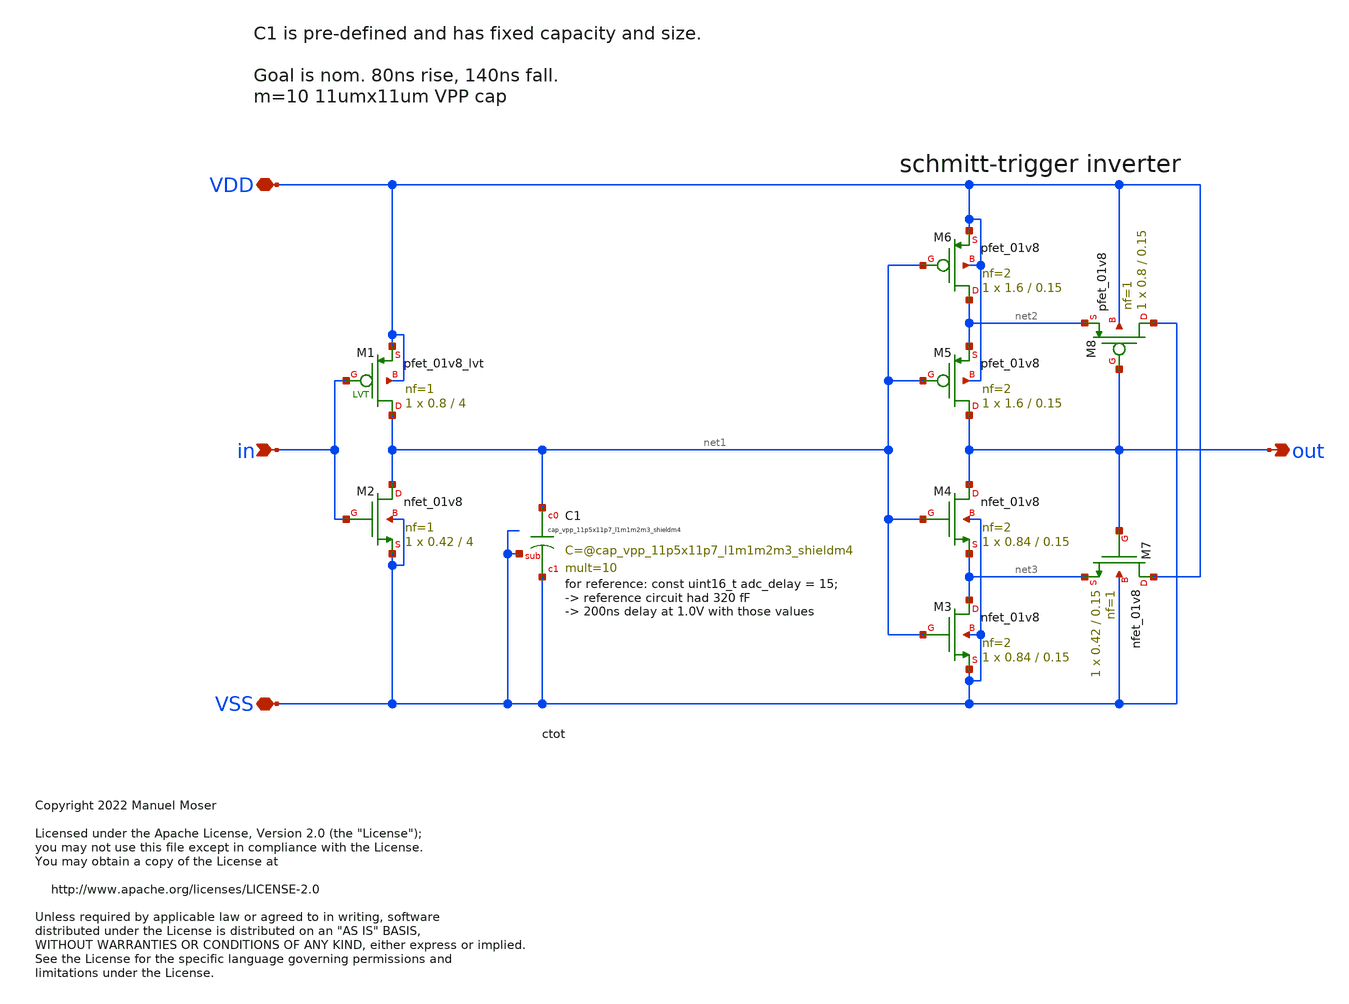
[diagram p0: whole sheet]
** sch_path: xschem/archive/adc_edge_detect_delay/_analog/adc_edge_detect_delay.sch
* Copyright 2022 Manuel Moser
* Licensed under the Apache License, Version 2.0 (the "License");
**.subckt adc_edge_detect_delay VDD VSS in out
*.iopin VDD
*.iopin VSS
*.ipin in
*.opin out
XC1 net1 VSS VSS sky130_fd_pr__cap_vpp_11p5x11p7_l1m1m2m3_shieldm4 mult=10 m=10
XM3 net3 net1 VSS VSS sky130_fd_pr__nfet_01v8 L=0.15 W=0.84 nf=2 ad='int((nf+1)/2) * W/nf * 0.29' as='int((nf+2)/2) * W/nf * 0.29'
+ pd='2*int((nf+1)/2) * (W/nf + 0.29)' ps='2*int((nf+2)/2) * (W/nf + 0.29)' nrd='0.29 / W' nrs='0.29 / W'
+ sa=0 sb=0 sd=0 mult=1 m=1
XM4 out net1 net3 VSS sky130_fd_pr__nfet_01v8 L=0.15 W=0.84 nf=2 ad='int((nf+1)/2) * W/nf * 0.29' as='int((nf+2)/2) * W/nf * 0.29'
+ pd='2*int((nf+1)/2) * (W/nf + 0.29)' ps='2*int((nf+2)/2) * (W/nf + 0.29)' nrd='0.29 / W' nrs='0.29 / W'
+ sa=0 sb=0 sd=0 mult=1 m=1
XM5 out net1 net2 VDD sky130_fd_pr__pfet_01v8 L=0.15 W=1.6 nf=2 ad='int((nf+1)/2) * W/nf * 0.29' as='int((nf+2)/2) * W/nf * 0.29'
+ pd='2*int((nf+1)/2) * (W/nf + 0.29)' ps='2*int((nf+2)/2) * (W/nf + 0.29)' nrd='0.29 / W' nrs='0.29 / W'
+ sa=0 sb=0 sd=0 mult=1 m=1
XM6 net2 net1 VDD VDD sky130_fd_pr__pfet_01v8 L=0.15 W=1.6 nf=2 ad='int((nf+1)/2) * W/nf * 0.29' as='int((nf+2)/2) * W/nf * 0.29'
+ pd='2*int((nf+1)/2) * (W/nf + 0.29)' ps='2*int((nf+2)/2) * (W/nf + 0.29)' nrd='0.29 / W' nrs='0.29 / W'
+ sa=0 sb=0 sd=0 mult=1 m=1
XM7 VDD out net3 VSS sky130_fd_pr__nfet_01v8 L=0.15 W=0.42 nf=1 ad='int((nf+1)/2) * W/nf * 0.29' as='int((nf+2)/2) * W/nf * 0.29'
+ pd='2*int((nf+1)/2) * (W/nf + 0.29)' ps='2*int((nf+2)/2) * (W/nf + 0.29)' nrd='0.29 / W' nrs='0.29 / W'
+ sa=0 sb=0 sd=0 mult=1 m=1
XM8 VSS out net2 VDD sky130_fd_pr__pfet_01v8 L=0.15 W=0.8 nf=1 ad='int((nf+1)/2) * W/nf * 0.29' as='int((nf+2)/2) * W/nf * 0.29'
+ pd='2*int((nf+1)/2) * (W/nf + 0.29)' ps='2*int((nf+2)/2) * (W/nf + 0.29)' nrd='0.29 / W' nrs='0.29 / W'
+ sa=0 sb=0 sd=0 mult=1 m=1
XM2 net1 in VSS VSS sky130_fd_pr__nfet_01v8 L=4 W=0.42 nf=1 ad='int((nf+1)/2) * W/nf * 0.29' as='int((nf+2)/2) * W/nf * 0.29'
+ pd='2*int((nf+1)/2) * (W/nf + 0.29)' ps='2*int((nf+2)/2) * (W/nf + 0.29)' nrd='0.29 / W' nrs='0.29 / W'
+ sa=0 sb=0 sd=0 mult=1 m=1
XM1 net1 in VDD VDD sky130_fd_pr__pfet_01v8_lvt L=4 W=0.8 nf=1 ad='int((nf+1)/2) * W/nf * 0.29' as='int((nf+2)/2) * W/nf * 0.29'
+ pd='2*int((nf+1)/2) * (W/nf + 0.29)' ps='2*int((nf+2)/2) * (W/nf + 0.29)' nrd='0.29 / W' nrs='0.29 / W'
+ sa=0 sb=0 sd=0 mult=1 m=1
**.ends
.end
